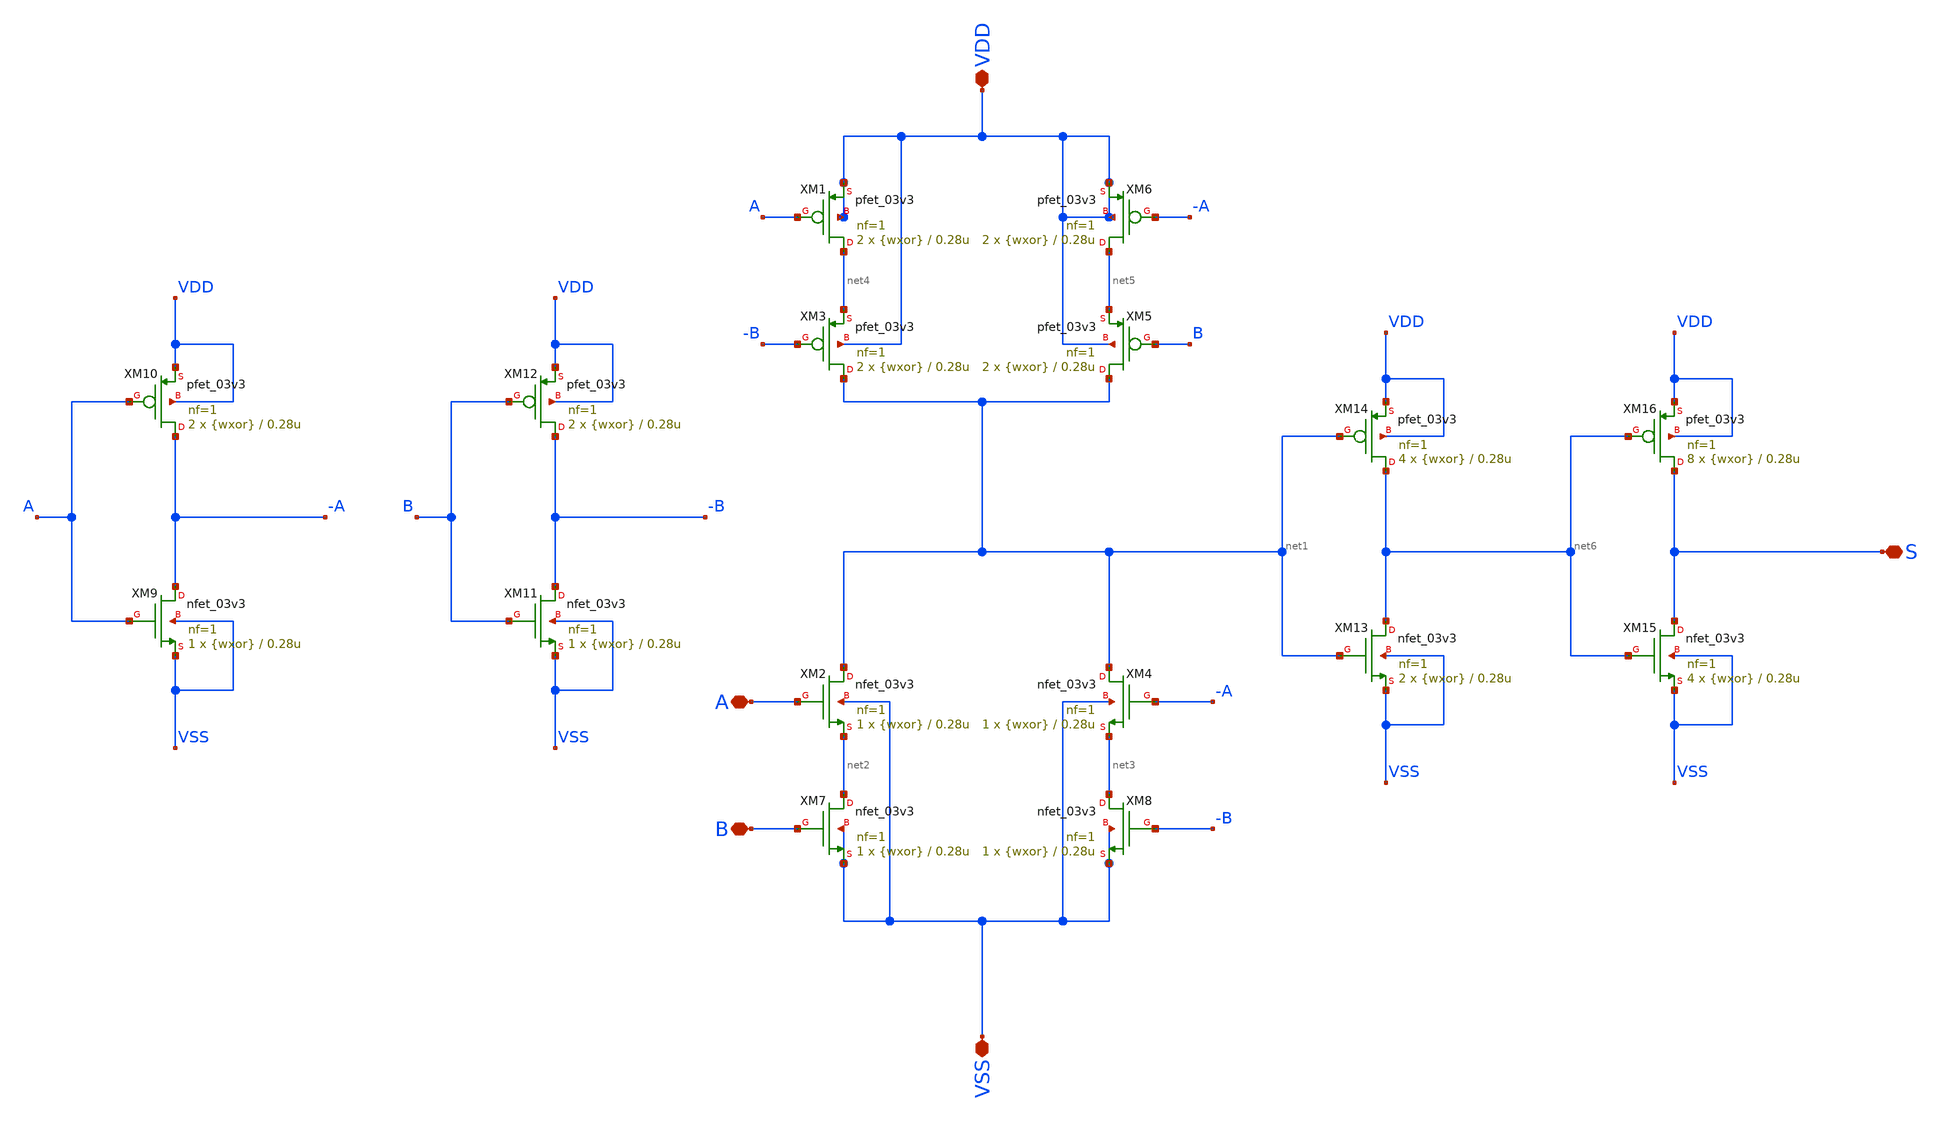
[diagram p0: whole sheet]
** sch_path: designs/ring_oscillator_pg/xor.sch
**.subckt xor VSS VDD S A B
*.iopin VSS
*.iopin VDD
*.iopin S
*.iopin A
*.iopin B
XM2 net1 A net2 VSS nfet_03v3 L=0.28u W={wxor} nf=1 ad='int((nf+1)/2) * W/nf * 0.18u' as='int((nf+2)/2) * W/nf * 0.18u'
+ pd='2*int((nf+1)/2) * (W/nf + 0.18u)' ps='2*int((nf+2)/2) * (W/nf + 0.18u)' nrd='0.18u / W' nrs='0.18u / W'
+ sa=0 sb=0 sd=0 m=1
XM3 net1 -B net4 VDD pfet_03v3 L=0.28u W={wxor} nf=1 ad='int((nf+1)/2) * W/nf * 0.18u' as='int((nf+2)/2) * W/nf * 0.18u'
+ pd='2*int((nf+1)/2) * (W/nf + 0.18u)' ps='2*int((nf+2)/2) * (W/nf + 0.18u)' nrd='0.18u / W' nrs='0.18u / W'
+ sa=0 sb=0 sd=0 m=2
XM1 net4 A VDD VDD pfet_03v3 L=0.28u W={wxor} nf=1 ad='int((nf+1)/2) * W/nf * 0.18u' as='int((nf+2)/2) * W/nf * 0.18u'
+ pd='2*int((nf+1)/2) * (W/nf + 0.18u)' ps='2*int((nf+2)/2) * (W/nf + 0.18u)' nrd='0.18u / W' nrs='0.18u / W'
+ sa=0 sb=0 sd=0 m=2
XM4 net1 -A net3 VSS nfet_03v3 L=0.28u W={wxor} nf=1 ad='int((nf+1)/2) * W/nf * 0.18u' as='int((nf+2)/2) * W/nf * 0.18u'
+ pd='2*int((nf+1)/2) * (W/nf + 0.18u)' ps='2*int((nf+2)/2) * (W/nf + 0.18u)' nrd='0.18u / W' nrs='0.18u / W'
+ sa=0 sb=0 sd=0 m=1
XM5 net1 B net5 VDD pfet_03v3 L=0.28u W={wxor} nf=1 ad='int((nf+1)/2) * W/nf * 0.18u' as='int((nf+2)/2) * W/nf * 0.18u'
+ pd='2*int((nf+1)/2) * (W/nf + 0.18u)' ps='2*int((nf+2)/2) * (W/nf + 0.18u)' nrd='0.18u / W' nrs='0.18u / W'
+ sa=0 sb=0 sd=0 m=2
XM6 net5 -A VDD VDD pfet_03v3 L=0.28u W={wxor} nf=1 ad='int((nf+1)/2) * W/nf * 0.18u' as='int((nf+2)/2) * W/nf * 0.18u'
+ pd='2*int((nf+1)/2) * (W/nf + 0.18u)' ps='2*int((nf+2)/2) * (W/nf + 0.18u)' nrd='0.18u / W' nrs='0.18u / W'
+ sa=0 sb=0 sd=0 m=2
XM7 net2 B VSS VSS nfet_03v3 L=0.28u W={wxor} nf=1 ad='int((nf+1)/2) * W/nf * 0.18u' as='int((nf+2)/2) * W/nf * 0.18u'
+ pd='2*int((nf+1)/2) * (W/nf + 0.18u)' ps='2*int((nf+2)/2) * (W/nf + 0.18u)' nrd='0.18u / W' nrs='0.18u / W'
+ sa=0 sb=0 sd=0 m=1
XM8 net3 -B VSS VSS nfet_03v3 L=0.28u W={wxor} nf=1 ad='int((nf+1)/2) * W/nf * 0.18u' as='int((nf+2)/2) * W/nf * 0.18u'
+ pd='2*int((nf+1)/2) * (W/nf + 0.18u)' ps='2*int((nf+2)/2) * (W/nf + 0.18u)' nrd='0.18u / W' nrs='0.18u / W'
+ sa=0 sb=0 sd=0 m=1
XM9 -A A VSS VSS nfet_03v3 L=0.28u W={wxor} nf=1 ad='int((nf+1)/2) * W/nf * 0.18u' as='int((nf+2)/2) * W/nf * 0.18u'
+ pd='2*int((nf+1)/2) * (W/nf + 0.18u)' ps='2*int((nf+2)/2) * (W/nf + 0.18u)' nrd='0.18u / W' nrs='0.18u / W'
+ sa=0 sb=0 sd=0 m=1
XM10 -A A VDD VDD pfet_03v3 L=0.28u W={wxor} nf=1 ad='int((nf+1)/2) * W/nf * 0.18u' as='int((nf+2)/2) * W/nf * 0.18u'
+ pd='2*int((nf+1)/2) * (W/nf + 0.18u)' ps='2*int((nf+2)/2) * (W/nf + 0.18u)' nrd='0.18u / W' nrs='0.18u / W'
+ sa=0 sb=0 sd=0 m=2
XM11 -B B VSS VSS nfet_03v3 L=0.28u W={wxor} nf=1 ad='int((nf+1)/2) * W/nf * 0.18u' as='int((nf+2)/2) * W/nf * 0.18u'
+ pd='2*int((nf+1)/2) * (W/nf + 0.18u)' ps='2*int((nf+2)/2) * (W/nf + 0.18u)' nrd='0.18u / W' nrs='0.18u / W'
+ sa=0 sb=0 sd=0 m=1
XM12 -B B VDD VDD pfet_03v3 L=0.28u W={wxor} nf=1 ad='int((nf+1)/2) * W/nf * 0.18u' as='int((nf+2)/2) * W/nf * 0.18u'
+ pd='2*int((nf+1)/2) * (W/nf + 0.18u)' ps='2*int((nf+2)/2) * (W/nf + 0.18u)' nrd='0.18u / W' nrs='0.18u / W'
+ sa=0 sb=0 sd=0 m=2
XM13 net6 net1 VSS VSS nfet_03v3 L=0.28u W={wxor} nf=1 ad='int((nf+1)/2) * W/nf * 0.18u' as='int((nf+2)/2) * W/nf * 0.18u'
+ pd='2*int((nf+1)/2) * (W/nf + 0.18u)' ps='2*int((nf+2)/2) * (W/nf + 0.18u)' nrd='0.18u / W' nrs='0.18u / W'
+ sa=0 sb=0 sd=0 m=2
XM14 net6 net1 VDD VDD pfet_03v3 L=0.28u W={wxor} nf=1 ad='int((nf+1)/2) * W/nf * 0.18u' as='int((nf+2)/2) * W/nf * 0.18u'
+ pd='2*int((nf+1)/2) * (W/nf + 0.18u)' ps='2*int((nf+2)/2) * (W/nf + 0.18u)' nrd='0.18u / W' nrs='0.18u / W'
+ sa=0 sb=0 sd=0 m=4
XM15 S net6 VSS VSS nfet_03v3 L=0.28u W={wxor} nf=1 ad='int((nf+1)/2) * W/nf * 0.18u' as='int((nf+2)/2) * W/nf * 0.18u'
+ pd='2*int((nf+1)/2) * (W/nf + 0.18u)' ps='2*int((nf+2)/2) * (W/nf + 0.18u)' nrd='0.18u / W' nrs='0.18u / W'
+ sa=0 sb=0 sd=0 m=4
XM16 S net6 VDD VDD pfet_03v3 L=0.28u W={wxor} nf=1 ad='int((nf+1)/2) * W/nf * 0.18u' as='int((nf+2)/2) * W/nf * 0.18u'
+ pd='2*int((nf+1)/2) * (W/nf + 0.18u)' ps='2*int((nf+2)/2) * (W/nf + 0.18u)' nrd='0.18u / W' nrs='0.18u / W'
+ sa=0 sb=0 sd=0 m=8
**.ends
.end
